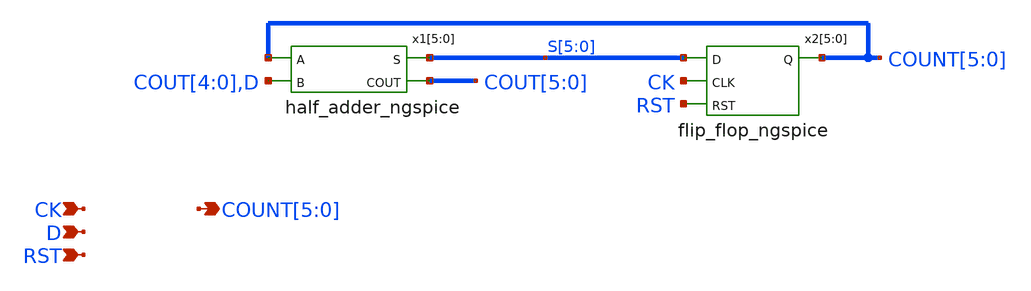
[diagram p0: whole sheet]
** sch_path: xschem-src/xschem_library/ngspice/counter_6bit_ngspice.sch
* Copyright (C) 1998-2026 Stefan Frederik Schippers
* This program is free software; you can redistribute it and/or modify
* it under the terms of the GNU General Public License as published by
* the Free Software Foundation; either version 2 of the License, or
* (at your option) any later version.
* This program is distributed in the hope that it will be useful,
* but WITHOUT ANY WARRANTY; without even the implied warranty of
* MERCHANTABILITY or FITNESS FOR A PARTICULAR PURPOSE.  See the
* GNU General Public License for more details.
* You should have received a copy of the GNU General Public License
* along with this program; if not, write to the Free Software
**.subckt counter_6bit_ngspice RST D COUNT[5],COUNT[4],COUNT[3],COUNT[2],COUNT[1],COUNT[0] CK
*.ipin RST
*.ipin D
*.opin COUNT[5],COUNT[4],COUNT[3],COUNT[2],COUNT[1],COUNT[0]
*.ipin CK
x2[5] S[5] CK COUNT[5] RST flip_flop_ngspice
x2[4] S[4] CK COUNT[4] RST flip_flop_ngspice
x2[3] S[3] CK COUNT[3] RST flip_flop_ngspice
x2[2] S[2] CK COUNT[2] RST flip_flop_ngspice
x2[1] S[1] CK COUNT[1] RST flip_flop_ngspice
x2[0] S[0] CK COUNT[0] RST flip_flop_ngspice
x1[5] COUNT[5] S[5] COUT[5] COUT[4] half_adder_ngspice
x1[4] COUNT[4] S[4] COUT[4] COUT[3] half_adder_ngspice
x1[3] COUNT[3] S[3] COUT[3] COUT[2] half_adder_ngspice
x1[2] COUNT[2] S[2] COUT[2] COUT[1] half_adder_ngspice
x1[1] COUNT[1] S[1] COUT[1] COUT[0] half_adder_ngspice
x1[0] COUNT[0] S[0] COUT[0] D half_adder_ngspice
**.ends

* expanding   symbol:  flip_flop_ngspice.sym # of pins=4
** sym_path: xschem-src/xschem_library/ngspice/flip_flop_ngspice.sym
** sch_path: xschem-src/xschem_library/ngspice/flip_flop_ngspice.sch
.subckt flip_flop_ngspice D CLK Q RST
*.ipin D
*.ipin CLK
*.ipin RST
*.opin Q
x2 DI keeper_ngspice
S1 net2 net3 VCC CLK SWITCH
S2 QI net1 CLK 0 SWITCH
x3 QI keeper_ngspice
x4 Q QI buf_ngspice RUP=100 RDOWN=100
S3 QI 0 RST 0 SWITCH
x1 net1 DI buf_ngspice RUP=1000 RDOWN=1000
S4 DI net2 VCC RST SWITCH
S5 DI 0 RST 0 SWITCH
x5 net3 D buf_ngspice RUP=1000 RDOWN=1000
.ends


* expanding   symbol:  half_adder_ngspice.sym # of pins=4
** sym_path: xschem-src/xschem_library/ngspice/half_adder_ngspice.sym
** sch_path: xschem-src/xschem_library/ngspice/half_adder_ngspice.sch
.subckt half_adder_ngspice A S COUT B
*.ipin A
*.ipin B
*.opin S
*.opin COUT
x1 S A B xor_ngspice ROUT=1000
x2 COUT A B and_ngspice ROUT=1000
.ends


* expanding   symbol:  keeper_ngspice.sym # of pins=1
** sym_path: xschem-src/xschem_library/ngspice/keeper_ngspice.sym
** sch_path: xschem-src/xschem_library/ngspice/keeper_ngspice.sch
.subckt keeper_ngspice A
*.ipin A
x1 Y A inv_ngspice RUP=2000 RDOWN=1000
x2 A Y inv_ngspice RUP=300k RDOWN=200k
.ends


* expanding   symbol:  buf_ngspice.sym # of pins=2
** sym_path: xschem-src/xschem_library/ngspice/buf_ngspice.sym
** sch_path: xschem-src/xschem_library/ngspice/buf_ngspice.sch
.subckt buf_ngspice Y A  RUP=2000 RDOWN=1000
*.ipin A
*.opin Y
B1 X1 0 V = 'VCC/2*(1+tanh((V(A1)-VCC/2)*100))'
C3 Y1 0 8f m=1
C1 A1 0 4f m=1
V1 Y Y1 0
V2 A1 A 0
B2 X1 Y1 I = 'v(X1,Y1) > 0 ? v(X1,Y1) / RUP : v(X1,Y1) / RDOWN'
.ends


* expanding   symbol:  xor_ngspice.sym # of pins=3
** sym_path: xschem-src/xschem_library/ngspice/xor_ngspice.sym
** sch_path: xschem-src/xschem_library/ngspice/xor_ngspice.sch
.subckt xor_ngspice Y A B  ROUT=1000
*.ipin A
*.opin Y
*.ipin B
B1 net1 0 V = 'VCC/2*(1+tanh((abs(V(A1)-V(B1))-VCC/2)*100))'
R1 Y1 net1 'ROUT' m=1
C1 A1 0 8f m=1
C2 B1 0 8f m=1
C3 Y1 0 8f m=1
V1 A1 A 0
V2 B1 B 0
V3 Y Y1 0
.ends


* expanding   symbol:  and_ngspice.sym # of pins=3
** sym_path: xschem-src/xschem_library/ngspice/and_ngspice.sym
** sch_path: xschem-src/xschem_library/ngspice/and_ngspice.sch
.subckt and_ngspice Y A B  ROUT=1000
*.ipin A
*.opin Y
*.ipin B
B1 net1 0 V = 'VCC/2*(1+tanh((min(V(A1),V(B1))-VCC/2)*100))'
R1 Y1 net1 'ROUT' m=1
C1 A1 0 8f m=1
C2 B1 0 8f m=1
C3 Y1 0 8f m=1
V1 A1 A 0
V2 B1 B 0
V3 Y Y1 0
.ends


* expanding   symbol:  inv_ngspice.sym # of pins=2
** sym_path: xschem-src/xschem_library/ngspice/inv_ngspice.sym
** sch_path: xschem-src/xschem_library/ngspice/inv_ngspice.sch
.subckt inv_ngspice Y A  RUP=2000 RDOWN=1000
*.ipin A
*.opin Y
B1 X1 0 V = 'VCC/2*(1-tanh((V(A1)-VCC/2)*100))'
C1 A1 0 8f m=1
C2 Y1 0 8f m=1
V1 Y Y1 0
.save i(v1)
V2 A1 A 0
.save i(v2)
B2 X1 Y1 I = 'v(X1,Y1) > 0 ? v(X1,Y1) / RUP : v(X1,Y1) / RDOWN'
.ends

.end
